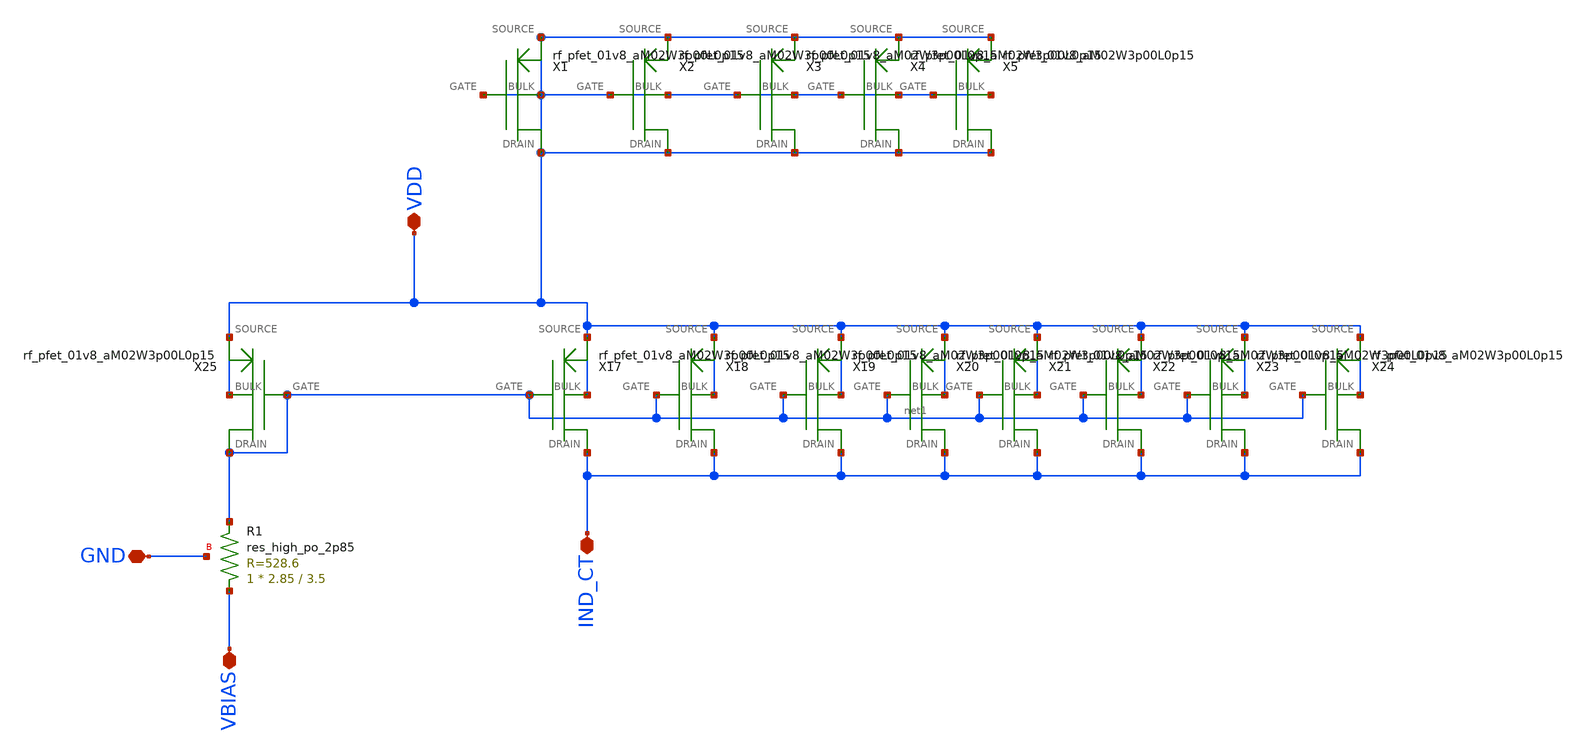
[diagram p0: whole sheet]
** sch_path: xschem/vco_pmirr.sch
**.subckt vco_pmirr IND_CT VBIAS VDD GND
*.iopin IND_CT
*.iopin VBIAS
*.iopin VDD
*.iopin GND
X25 VDD net1 net1 VDD rf_pfet_01v8_aM02W3p00L0p15
X17 VDD net1 IND_CT VDD rf_pfet_01v8_aM02W3p00L0p15
X18 VDD net1 IND_CT VDD rf_pfet_01v8_aM02W3p00L0p15
X19 VDD net1 IND_CT VDD rf_pfet_01v8_aM02W3p00L0p15
X20 VDD net1 IND_CT VDD rf_pfet_01v8_aM02W3p00L0p15
X21 VDD net1 IND_CT VDD rf_pfet_01v8_aM02W3p00L0p15
X22 VDD net1 IND_CT VDD rf_pfet_01v8_aM02W3p00L0p15
X23 VDD net1 IND_CT VDD rf_pfet_01v8_aM02W3p00L0p15
X24 VDD net1 IND_CT VDD rf_pfet_01v8_aM02W3p00L0p15
X1 VDD VDD VDD VDD rf_pfet_01v8_aM02W3p00L0p15
X2 VDD VDD VDD VDD rf_pfet_01v8_aM02W3p00L0p15
X3 VDD VDD VDD VDD rf_pfet_01v8_aM02W3p00L0p15
X4 VDD VDD VDD VDD rf_pfet_01v8_aM02W3p00L0p15
X5 VDD VDD VDD VDD rf_pfet_01v8_aM02W3p00L0p15
XR1 VBIAS net1 GND sky130_fd_pr__res_high_po_2p85 L=3.5 mult=1 m=1
**.ends
.end
